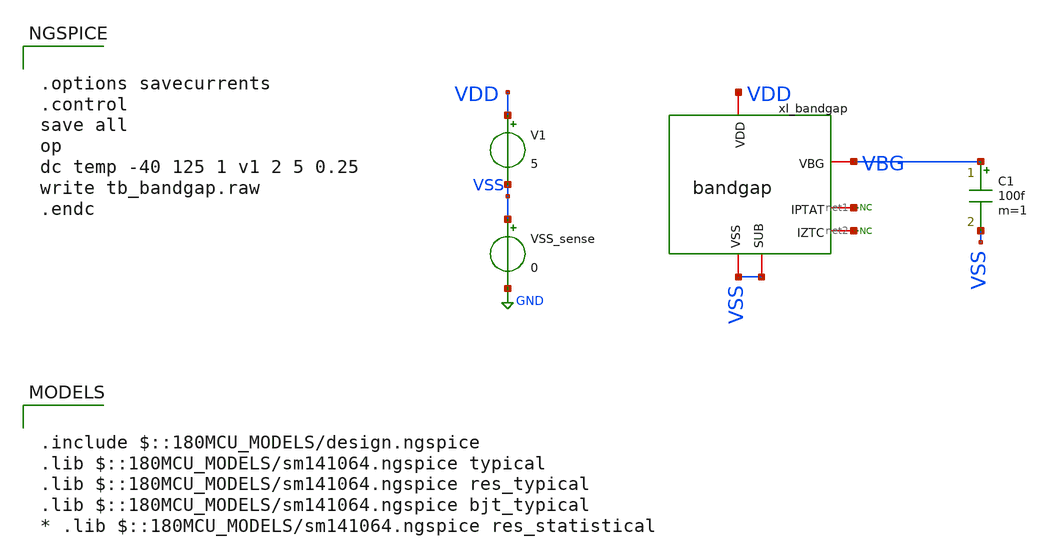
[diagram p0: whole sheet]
** sch_path: designs/libs/tb_bandgap/tb_bandgap/tb_bandgap.sch
**.subckt tb_bandgap
V1 VDD VSS 5
VSS_sense VSS GND 0
C1 VBG VSS 100f m=1
* noconn #net1
* noconn #net2
xI_bandgap VDD VBG net1 net2 VSS VSS bandgap
**** begin user architecture code

.include $::180MCU_MODELS/design.ngspice
.lib $::180MCU_MODELS/sm141064.ngspice typical
.lib $::180MCU_MODELS/sm141064.ngspice res_typical
.lib $::180MCU_MODELS/sm141064.ngspice bjt_typical
* .lib $::180MCU_MODELS/sm141064.ngspice res_statistical



.options savecurrents
.control
save all
op
dc temp -40 125 1 v1 2 5 0.25
write tb_bandgap.raw
.endc


**** end user architecture code
**.ends

* expanding   symbol:  libs/core_bandgap/bandgap/bandgap.sym # of pins=6
** sym_path: designs/libs/core_bandgap/bandgap/bandgap.sym
** sch_path: designs/libs/core_bandgap/bandgap/bandgap.sch
.subckt bandgap VDD VBG IPTAT IZTC SUB VSS
*.iopin VDD
*.iopin VSS
*.iopin SUB
*.iopin VBG
*.iopin IPTAT
*.iopin IZTC
* noconn SUB
XQ1 VSS VSS vbe pnp_05p00x00p42 m=2 par=2
XQ2 VSS VSS vbjt_ptat[0] pnp_05p00x00p42 m=16 par=16
XMpref1 net2 vpref VDD VDD pfet_05v0 L=0.8u W=3.2u nf=1 ad='int((nf+1)/2) * W/nf * 0.18u' as='int((nf+2)/2) * W/nf * 0.18u'
+ pd='2*int((nf+1)/2) * (W/nf + 0.18u)' ps='2*int((nf+2)/2) * (W/nf + 0.18u)' nrd='0.18u / W' nrs='0.18u / W'
+ sa=0 sb=0 sd=0 m=2
XMnref1 net6 vnref vbjt_ptat[6] VSS nfet_05v0 L=1u W=1u nf=1 ad='int((nf+1)/2) * W/nf * 0.18u' as='int((nf+2)/2) * W/nf * 0.18u'
+ pd='2*int((nf+1)/2) * (W/nf + 0.18u)' ps='2*int((nf+2)/2) * (W/nf + 0.18u)' nrd='0.18u / W' nrs='0.18u / W'
+ sa=0 sb=0 sd=0 m=4
XMnref2 net5 vnref vbe VSS nfet_05v0 L=1u W=1u nf=1 ad='int((nf+1)/2) * W/nf * 0.18u' as='int((nf+2)/2) * W/nf * 0.18u'
+ pd='2*int((nf+1)/2) * (W/nf + 0.18u)' ps='2*int((nf+2)/2) * (W/nf + 0.18u)' nrd='0.18u / W' nrs='0.18u / W'
+ sa=0 sb=0 sd=0 m=4
XMpref2 net1 vpref VDD VDD pfet_05v0 L=0.8u W=3.2u nf=1 ad='int((nf+1)/2) * W/nf * 0.18u' as='int((nf+2)/2) * W/nf * 0.18u'
+ pd='2*int((nf+1)/2) * (W/nf + 0.18u)' ps='2*int((nf+2)/2) * (W/nf + 0.18u)' nrd='0.18u / W' nrs='0.18u / W'
+ sa=0 sb=0 sd=0 m=2
XRptat[5] vbjt_ptat[5] vbjt_ptat[6] VDD ppolyf_u_1k r_width=1e-6 r_length=4.5e-6 m=1
XRptat[4] vbjt_ptat[4] vbjt_ptat[5] VDD ppolyf_u_1k r_width=1e-6 r_length=4.5e-6 m=1
XRptat[3] vbjt_ptat[3] vbjt_ptat[4] VDD ppolyf_u_1k r_width=1e-6 r_length=4.5e-6 m=1
XRptat[2] vbjt_ptat[2] vbjt_ptat[3] VDD ppolyf_u_1k r_width=1e-6 r_length=4.5e-6 m=1
XRptat[1] vbjt_ptat[1] vbjt_ptat[2] VDD ppolyf_u_1k r_width=1e-6 r_length=4.5e-6 m=1
XRptat[0] vbjt_ptat[0] vbjt_ptat[1] VDD ppolyf_u_1k r_width=1e-6 r_length=4.5e-6 m=1
* tap: vbjt_ptat[5:0] --> vbjt_ptat[0]
* tap: vbjt_ptat[6:1] --> vbjt_ptat[6]
XQ3 VSS VSS vbjt_bg[0] pnp_05p00x00p42 m=2 par=2
XMpref3 net3 vpref VDD VDD pfet_05v0 L=0.8u W=3.2u nf=1 ad='int((nf+1)/2) * W/nf * 0.18u' as='int((nf+2)/2) * W/nf * 0.18u'
+ pd='2*int((nf+1)/2) * (W/nf + 0.18u)' ps='2*int((nf+2)/2) * (W/nf + 0.18u)' nrd='0.18u / W' nrs='0.18u / W'
+ sa=0 sb=0 sd=0 m=2
XRref[50] vbjt_bg[50] VBG VDD ppolyf_u_1k r_width=1e-6 r_length=4.5e-6 m=1
XRref[49] vbjt_bg[49] vbjt_bg[50] VDD ppolyf_u_1k r_width=1e-6 r_length=4.5e-6 m=1
XRref[48] vbjt_bg[48] vbjt_bg[49] VDD ppolyf_u_1k r_width=1e-6 r_length=4.5e-6 m=1
XRref[47] vbjt_bg[47] vbjt_bg[48] VDD ppolyf_u_1k r_width=1e-6 r_length=4.5e-6 m=1
XRref[46] vbjt_bg[46] vbjt_bg[47] VDD ppolyf_u_1k r_width=1e-6 r_length=4.5e-6 m=1
XRref[45] vbjt_bg[45] vbjt_bg[46] VDD ppolyf_u_1k r_width=1e-6 r_length=4.5e-6 m=1
XRref[44] vbjt_bg[44] vbjt_bg[45] VDD ppolyf_u_1k r_width=1e-6 r_length=4.5e-6 m=1
XRref[43] vbjt_bg[43] vbjt_bg[44] VDD ppolyf_u_1k r_width=1e-6 r_length=4.5e-6 m=1
XRref[42] vbjt_bg[42] vbjt_bg[43] VDD ppolyf_u_1k r_width=1e-6 r_length=4.5e-6 m=1
XRref[41] vbjt_bg[41] vbjt_bg[42] VDD ppolyf_u_1k r_width=1e-6 r_length=4.5e-6 m=1
XRref[40] vbjt_bg[40] vbjt_bg[41] VDD ppolyf_u_1k r_width=1e-6 r_length=4.5e-6 m=1
XRref[39] vbjt_bg[39] vbjt_bg[40] VDD ppolyf_u_1k r_width=1e-6 r_length=4.5e-6 m=1
XRref[38] vbjt_bg[38] vbjt_bg[39] VDD ppolyf_u_1k r_width=1e-6 r_length=4.5e-6 m=1
XRref[37] vbjt_bg[37] vbjt_bg[38] VDD ppolyf_u_1k r_width=1e-6 r_length=4.5e-6 m=1
XRref[36] vbjt_bg[36] vbjt_bg[37] VDD ppolyf_u_1k r_width=1e-6 r_length=4.5e-6 m=1
XRref[35] vbjt_bg[35] vbjt_bg[36] VDD ppolyf_u_1k r_width=1e-6 r_length=4.5e-6 m=1
XRref[34] vbjt_bg[34] vbjt_bg[35] VDD ppolyf_u_1k r_width=1e-6 r_length=4.5e-6 m=1
XRref[33] vbjt_bg[33] vbjt_bg[34] VDD ppolyf_u_1k r_width=1e-6 r_length=4.5e-6 m=1
XRref[32] vbjt_bg[32] vbjt_bg[33] VDD ppolyf_u_1k r_width=1e-6 r_length=4.5e-6 m=1
XRref[31] vbjt_bg[31] vbjt_bg[32] VDD ppolyf_u_1k r_width=1e-6 r_length=4.5e-6 m=1
XRref[30] vbjt_bg[30] vbjt_bg[31] VDD ppolyf_u_1k r_width=1e-6 r_length=4.5e-6 m=1
XRref[29] vbjt_bg[29] vbjt_bg[30] VDD ppolyf_u_1k r_width=1e-6 r_length=4.5e-6 m=1
XRref[28] vbjt_bg[28] vbjt_bg[29] VDD ppolyf_u_1k r_width=1e-6 r_length=4.5e-6 m=1
XRref[27] vbjt_bg[27] vbjt_bg[28] VDD ppolyf_u_1k r_width=1e-6 r_length=4.5e-6 m=1
XRref[26] vbjt_bg[26] vbjt_bg[27] VDD ppolyf_u_1k r_width=1e-6 r_length=4.5e-6 m=1
XRref[25] vbjt_bg[25] vbjt_bg[26] VDD ppolyf_u_1k r_width=1e-6 r_length=4.5e-6 m=1
XRref[24] vbjt_bg[24] vbjt_bg[25] VDD ppolyf_u_1k r_width=1e-6 r_length=4.5e-6 m=1
XRref[23] vbjt_bg[23] vbjt_bg[24] VDD ppolyf_u_1k r_width=1e-6 r_length=4.5e-6 m=1
XRref[22] vbjt_bg[22] vbjt_bg[23] VDD ppolyf_u_1k r_width=1e-6 r_length=4.5e-6 m=1
XRref[21] vbjt_bg[21] vbjt_bg[22] VDD ppolyf_u_1k r_width=1e-6 r_length=4.5e-6 m=1
XRref[20] vbjt_bg[20] vbjt_bg[21] VDD ppolyf_u_1k r_width=1e-6 r_length=4.5e-6 m=1
XRref[19] vbjt_bg[19] vbjt_bg[20] VDD ppolyf_u_1k r_width=1e-6 r_length=4.5e-6 m=1
XRref[18] vbjt_bg[18] vbjt_bg[19] VDD ppolyf_u_1k r_width=1e-6 r_length=4.5e-6 m=1
XRref[17] vbjt_bg[17] vbjt_bg[18] VDD ppolyf_u_1k r_width=1e-6 r_length=4.5e-6 m=1
XRref[16] vbjt_bg[16] vbjt_bg[17] VDD ppolyf_u_1k r_width=1e-6 r_length=4.5e-6 m=1
XRref[15] vbjt_bg[15] vbjt_bg[16] VDD ppolyf_u_1k r_width=1e-6 r_length=4.5e-6 m=1
XRref[14] vbjt_bg[14] vbjt_bg[15] VDD ppolyf_u_1k r_width=1e-6 r_length=4.5e-6 m=1
XRref[13] vbjt_bg[13] vbjt_bg[14] VDD ppolyf_u_1k r_width=1e-6 r_length=4.5e-6 m=1
XRref[12] vbjt_bg[12] vbjt_bg[13] VDD ppolyf_u_1k r_width=1e-6 r_length=4.5e-6 m=1
XRref[11] vbjt_bg[11] vbjt_bg[12] VDD ppolyf_u_1k r_width=1e-6 r_length=4.5e-6 m=1
XRref[10] vbjt_bg[10] vbjt_bg[11] VDD ppolyf_u_1k r_width=1e-6 r_length=4.5e-6 m=1
XRref[9] vbjt_bg[9] vbjt_bg[10] VDD ppolyf_u_1k r_width=1e-6 r_length=4.5e-6 m=1
XRref[8] vbjt_bg[8] vbjt_bg[9] VDD ppolyf_u_1k r_width=1e-6 r_length=4.5e-6 m=1
XRref[7] vbjt_bg[7] vbjt_bg[8] VDD ppolyf_u_1k r_width=1e-6 r_length=4.5e-6 m=1
XRref[6] vbjt_bg[6] vbjt_bg[7] VDD ppolyf_u_1k r_width=1e-6 r_length=4.5e-6 m=1
XRref[5] vbjt_bg[5] vbjt_bg[6] VDD ppolyf_u_1k r_width=1e-6 r_length=4.5e-6 m=1
XRref[4] vbjt_bg[4] vbjt_bg[5] VDD ppolyf_u_1k r_width=1e-6 r_length=4.5e-6 m=1
XRref[3] vbjt_bg[3] vbjt_bg[4] VDD ppolyf_u_1k r_width=1e-6 r_length=4.5e-6 m=1
XRref[2] vbjt_bg[2] vbjt_bg[3] VDD ppolyf_u_1k r_width=1e-6 r_length=4.5e-6 m=1
XRref[1] vbjt_bg[1] vbjt_bg[2] VDD ppolyf_u_1k r_width=1e-6 r_length=4.5e-6 m=1
XRref[0] vbjt_bg[0] vbjt_bg[1] VDD ppolyf_u_1k r_width=1e-6 r_length=4.5e-6 m=1
* tap: vbjt_bg[50:0] --> vbjt_bg[0]
XMpref4 net4 vpref VDD VDD pfet_05v0 L=0.8u W=3.2u nf=1 ad='int((nf+1)/2) * W/nf * 0.18u' as='int((nf+2)/2) * W/nf * 0.18u'
+ pd='2*int((nf+1)/2) * (W/nf + 0.18u)' ps='2*int((nf+2)/2) * (W/nf + 0.18u)' nrd='0.18u / W' nrs='0.18u / W'
+ sa=0 sb=0 sd=0 m=2
* noconn IZTC
XMpref5 vpref vpcas net2 VDD pfet_05v0 L=0.8u W=3.2u nf=1 ad='int((nf+1)/2) * W/nf * 0.18u' as='int((nf+2)/2) * W/nf * 0.18u'
+ pd='2*int((nf+1)/2) * (W/nf + 0.18u)' ps='2*int((nf+2)/2) * (W/nf + 0.18u)' nrd='0.18u / W' nrs='0.18u / W'
+ sa=0 sb=0 sd=0 m=8
XMpref6 vncas vpcas net1 VDD pfet_05v0 L=0.8u W=3.2u nf=1 ad='int((nf+1)/2) * W/nf * 0.18u' as='int((nf+2)/2) * W/nf * 0.18u'
+ pd='2*int((nf+1)/2) * (W/nf + 0.18u)' ps='2*int((nf+2)/2) * (W/nf + 0.18u)' nrd='0.18u / W' nrs='0.18u / W'
+ sa=0 sb=0 sd=0 m=8
XMpref7 VBG vpcas net3 VDD pfet_05v0 L=0.8u W=3.2u nf=1 ad='int((nf+1)/2) * W/nf * 0.18u' as='int((nf+2)/2) * W/nf * 0.18u'
+ pd='2*int((nf+1)/2) * (W/nf + 0.18u)' ps='2*int((nf+2)/2) * (W/nf + 0.18u)' nrd='0.18u / W' nrs='0.18u / W'
+ sa=0 sb=0 sd=0 m=8
XMpref8 IPTAT vpref net4 VDD pfet_05v0 L=0.8u W=3.2u nf=1 ad='int((nf+1)/2) * W/nf * 0.18u' as='int((nf+2)/2) * W/nf * 0.18u'
+ pd='2*int((nf+1)/2) * (W/nf + 0.18u)' ps='2*int((nf+2)/2) * (W/nf + 0.18u)' nrd='0.18u / W' nrs='0.18u / W'
+ sa=0 sb=0 sd=0 m=8
XRpcas[15] vr_pcas[15] vpref VDD ppolyf_u_1k r_width=1e-6 r_length=4.5e-6 m=1
XRpcas[14] vr_pcas[14] vr_pcas[15] VDD ppolyf_u_1k r_width=1e-6 r_length=4.5e-6 m=1
XRpcas[13] vr_pcas[13] vr_pcas[14] VDD ppolyf_u_1k r_width=1e-6 r_length=4.5e-6 m=1
XRpcas[12] vr_pcas[12] vr_pcas[13] VDD ppolyf_u_1k r_width=1e-6 r_length=4.5e-6 m=1
XRpcas[11] vr_pcas[11] vr_pcas[12] VDD ppolyf_u_1k r_width=1e-6 r_length=4.5e-6 m=1
XRpcas[10] vr_pcas[10] vr_pcas[11] VDD ppolyf_u_1k r_width=1e-6 r_length=4.5e-6 m=1
XRpcas[9] vr_pcas[9] vr_pcas[10] VDD ppolyf_u_1k r_width=1e-6 r_length=4.5e-6 m=1
XRpcas[8] vr_pcas[8] vr_pcas[9] VDD ppolyf_u_1k r_width=1e-6 r_length=4.5e-6 m=1
XRpcas[7] vr_pcas[7] vr_pcas[8] VDD ppolyf_u_1k r_width=1e-6 r_length=4.5e-6 m=1
XRpcas[6] vr_pcas[6] vr_pcas[7] VDD ppolyf_u_1k r_width=1e-6 r_length=4.5e-6 m=1
XRpcas[5] vr_pcas[5] vr_pcas[6] VDD ppolyf_u_1k r_width=1e-6 r_length=4.5e-6 m=1
XRpcas[4] vr_pcas[4] vr_pcas[5] VDD ppolyf_u_1k r_width=1e-6 r_length=4.5e-6 m=1
XRpcas[3] vr_pcas[3] vr_pcas[4] VDD ppolyf_u_1k r_width=1e-6 r_length=4.5e-6 m=1
XRpcas[2] vr_pcas[2] vr_pcas[3] VDD ppolyf_u_1k r_width=1e-6 r_length=4.5e-6 m=1
XRpcas[1] vr_pcas[1] vr_pcas[2] VDD ppolyf_u_1k r_width=1e-6 r_length=4.5e-6 m=1
XRpcas[0] vpcas vr_pcas[1] VDD ppolyf_u_1k r_width=1e-6 r_length=4.5e-6 m=1
XMnref3 vpcas vncas net6 VSS nfet_05v0 L=0.8u W=8u nf=1 ad='int((nf+1)/2) * W/nf * 0.18u' as='int((nf+2)/2) * W/nf * 0.18u'
+ pd='2*int((nf+1)/2) * (W/nf + 0.18u)' ps='2*int((nf+2)/2) * (W/nf + 0.18u)' nrd='0.18u / W' nrs='0.18u / W'
+ sa=0 sb=0 sd=0 m=4
XMnref4 vnref vncas net5 VSS nfet_05v0 L=0.8u W=8u nf=1 ad='int((nf+1)/2) * W/nf * 0.18u' as='int((nf+2)/2) * W/nf * 0.18u'
+ pd='2*int((nf+1)/2) * (W/nf + 0.18u)' ps='2*int((nf+2)/2) * (W/nf + 0.18u)' nrd='0.18u / W' nrs='0.18u / W'
+ sa=0 sb=0 sd=0 m=4
XRncas1[2] vr_ncas[2] vncas VDD ppolyf_u_1k r_width=1e-6 r_length=4.5e-6 m=1
XRncas1[1] vr_ncas[1] vr_ncas[2] VDD ppolyf_u_1k r_width=1e-6 r_length=4.5e-6 m=1
XRncas1[0] vnref vr_ncas[1] VDD ppolyf_u_1k r_width=1e-6 r_length=4.5e-6 m=1
.ends

.GLOBAL GND
.end
